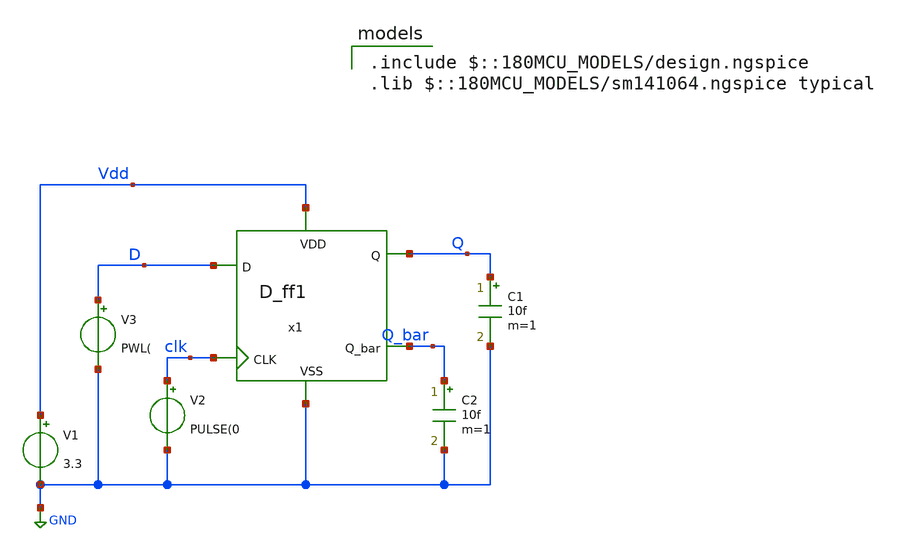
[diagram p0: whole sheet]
** sch_path: designs/libs/core_digital/TB_D_ff1.sch
**.subckt TB_D_ff1
V1 Vdd GND 3.3
C1 Q GND 10f m=1
C2 Q_bar GND 10f m=1
V2 clk GND PULSE(0
V3 D GND PWL(
x1 Vdd D Q Q_bar clk GND D_ff1
**** begin user architecture code

.include $::180MCU_MODELS/design.ngspice
.lib $::180MCU_MODELS/sm141064.ngspice typical

**** end user architecture code
**.ends
.GLOBAL GND
.end
